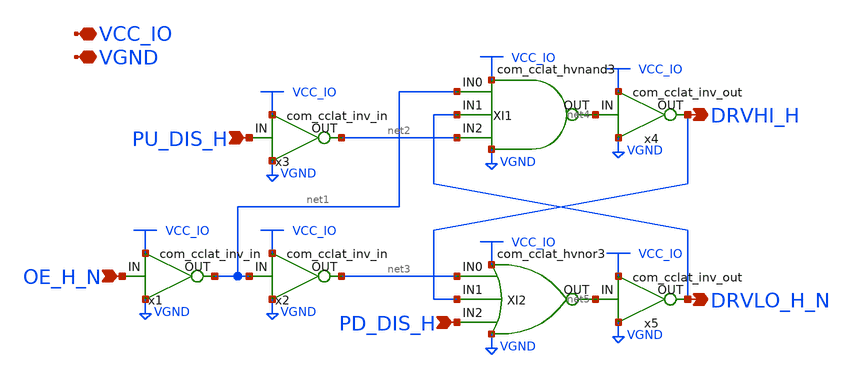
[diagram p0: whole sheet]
** sch_path: com_cclat.sch
* Copyright 2023 David Mitchell Bailey
* Licensed under the Apache License, Version 2.0 (the "License");
* you may not use this file except in compliance with the License.
* You may obtain a copy of the License at
* https://www.apache.org/licenses/LICENSE-2.0
* Unless required by applicable law or agreed to in writing, software
* distributed under the License is distributed on an "AS IS" BASIS,
* WITHOUT WARRANTIES OR CONDITIONS OF ANY KIND, either express or implied.
* See the License for the specific language governing permissions and
* limitations under the License.
**.subckt com_cclat PU_DIS_H VCC_IO DRVHI_H OE_H_N PD_DIS_H DRVLO_H_N VGND
*.ipin PU_DIS_H
*.iopin VCC_IO
*.opin DRVHI_H
*.ipin OE_H_N
*.ipin PD_DIS_H
*.opin DRVLO_H_N
*.iopin VGND
x1 OE_H_N net1 VCC_IO VGND com_cclat_inv_in
x2 net1 net3 VCC_IO VGND com_cclat_inv_in
x3 PU_DIS_H net2 VCC_IO VGND com_cclat_inv_in
XI1 net1 DRVLO_H_N net2 net4 VCC_IO VGND com_cclat_hvnand3
XI2 net3 DRVHI_H PD_DIS_H net5 VCC_IO VGND com_cclat_hvnor3
x4 net4 DRVHI_H VCC_IO VGND com_cclat_inv_out
x5 net5 DRVLO_H_N VCC_IO VGND com_cclat_inv_out
**.ends

* expanding   symbol:  com_cclat_inv_in.sym # of pins=4
** sym_path: com_cclat_inv_in.sym
** sch_path: com_cclat_inv_in.sch
.subckt com_cclat_inv_in IN OUT VCC_IO VGND
*.ipin IN
*.opin OUT
*.iopin VCC_IO
*.iopin VGND
XI1 OUT IN VGND VGND sky130_fd_pr__nfet_g5v0d10v5 L=0.6 W=3 nf=1 ad='int((nf+1)/2) * W/nf * 0.29' as='int((nf+2)/2) * W/nf * 0.29'
+ pd='2*int((nf+1)/2) * (W/nf + 0.29)' ps='2*int((nf+2)/2) * (W/nf + 0.29)' nrd='0.29 / W' nrs='0.29 / W'
+ sa=0 sb=0 sd=0 mult=1 m=1
XI2 OUT IN VCC_IO VCC_IO sky130_fd_pr__pfet_g5v0d10v5 L=0.5 W=5 nf=1 ad='int((nf+1)/2) * W/nf * 0.29'
+ as='int((nf+2)/2) * W/nf * 0.29' pd='2*int((nf+1)/2) * (W/nf + 0.29)' ps='2*int((nf+2)/2) * (W/nf + 0.29)'
+ nrd='0.29 / W' nrs='0.29 / W' sa=0 sb=0 sd=0 mult=1 m=1
.ends


* expanding   symbol:  com_cclat_hvnand3.sym # of pins=6
** sym_path: com_cclat_hvnand3.sym
** sch_path: com_cclat_hvnand3.sch
.subckt com_cclat_hvnand3 IN0 IN1 IN2 OUT VCC_IO VGND
*.ipin IN2
*.opin OUT
*.iopin VCC_IO
*.iopin VGND
*.ipin IN1
*.ipin IN0
XI1 OUT IN2 net1 VGND sky130_fd_pr__nfet_g5v0d10v5 L=0.6 W=3 nf=1 ad='int((nf+1)/2) * W/nf * 0.29' as='int((nf+2)/2) * W/nf * 0.29'
+ pd='2*int((nf+1)/2) * (W/nf + 0.29)' ps='2*int((nf+2)/2) * (W/nf + 0.29)' nrd='0.29 / W' nrs='0.29 / W'
+ sa=0 sb=0 sd=0 mult=2 m=2
XI5 OUT IN2 VCC_IO VCC_IO sky130_fd_pr__pfet_g5v0d10v5 L=0.5 W=5 nf=1 ad='int((nf+1)/2) * W/nf * 0.29'
+ as='int((nf+2)/2) * W/nf * 0.29' pd='2*int((nf+1)/2) * (W/nf + 0.29)' ps='2*int((nf+2)/2) * (W/nf + 0.29)'
+ nrd='0.29 / W' nrs='0.29 / W' sa=0 sb=0 sd=0 mult=1 m=1
XI3 OUT IN1 VCC_IO VCC_IO sky130_fd_pr__pfet_g5v0d10v5 L=0.5 W=5 nf=1 ad='int((nf+1)/2) * W/nf * 0.29'
+ as='int((nf+2)/2) * W/nf * 0.29' pd='2*int((nf+1)/2) * (W/nf + 0.29)' ps='2*int((nf+2)/2) * (W/nf + 0.29)'
+ nrd='0.29 / W' nrs='0.29 / W' sa=0 sb=0 sd=0 mult=1 m=1
XI6 net1 IN1 net2 VGND sky130_fd_pr__nfet_g5v0d10v5 L=0.6 W=3 nf=1 ad='int((nf+1)/2) * W/nf * 0.29' as='int((nf+2)/2) * W/nf * 0.29'
+ pd='2*int((nf+1)/2) * (W/nf + 0.29)' ps='2*int((nf+2)/2) * (W/nf + 0.29)' nrd='0.29 / W' nrs='0.29 / W'
+ sa=0 sb=0 sd=0 mult=2 m=2
XI2 net2 IN0 VGND VGND sky130_fd_pr__nfet_g5v0d10v5 L=0.6 W=3 nf=1 ad='int((nf+1)/2) * W/nf * 0.29' as='int((nf+2)/2) * W/nf * 0.29'
+ pd='2*int((nf+1)/2) * (W/nf + 0.29)' ps='2*int((nf+2)/2) * (W/nf + 0.29)' nrd='0.29 / W' nrs='0.29 / W'
+ sa=0 sb=0 sd=0 mult=4 m=4
XI4 OUT IN0 VCC_IO VCC_IO sky130_fd_pr__pfet_g5v0d10v5 L=0.5 W=5 nf=1 ad='int((nf+1)/2) * W/nf * 0.29'
+ as='int((nf+2)/2) * W/nf * 0.29' pd='2*int((nf+1)/2) * (W/nf + 0.29)' ps='2*int((nf+2)/2) * (W/nf + 0.29)'
+ nrd='0.29 / W' nrs='0.29 / W' sa=0 sb=0 sd=0 mult=1 m=1
.ends


* expanding   symbol:  com_cclat_hvnor3.sym # of pins=6
** sym_path: com_cclat_hvnor3.sym
** sch_path: com_cclat_hvnor3.sch
.subckt com_cclat_hvnor3 IN0 IN1 IN2 OUT VCC_IO VGND
*.ipin IN2
*.opin OUT
*.iopin VCC_IO
*.iopin VGND
*.ipin IN0
*.ipin IN1
XI2 OUT IN2 VGND VGND sky130_fd_pr__nfet_g5v0d10v5 L=0.6 W=3 nf=1 ad='int((nf+1)/2) * W/nf * 0.29' as='int((nf+2)/2) * W/nf * 0.29'
+ pd='2*int((nf+1)/2) * (W/nf + 0.29)' ps='2*int((nf+2)/2) * (W/nf + 0.29)' nrd='0.29 / W' nrs='0.29 / W'
+ sa=0 sb=0 sd=0 mult=2 m=2
XI1 OUT IN2 net1 VCC_IO sky130_fd_pr__pfet_g5v0d10v5 L=0.5 W=5 nf=1 ad='int((nf+1)/2) * W/nf * 0.29'
+ as='int((nf+2)/2) * W/nf * 0.29' pd='2*int((nf+1)/2) * (W/nf + 0.29)' ps='2*int((nf+2)/2) * (W/nf + 0.29)'
+ nrd='0.29 / W' nrs='0.29 / W' sa=0 sb=0 sd=0 mult=4 m=4
XI3 net2 IN0 VCC_IO VCC_IO sky130_fd_pr__pfet_g5v0d10v5 L=0.6 W=5 nf=1 ad='int((nf+1)/2) * W/nf * 0.29'
+ as='int((nf+2)/2) * W/nf * 0.29' pd='2*int((nf+1)/2) * (W/nf + 0.29)' ps='2*int((nf+2)/2) * (W/nf + 0.29)'
+ nrd='0.29 / W' nrs='0.29 / W' sa=0 sb=0 sd=0 mult=8 m=8
XI4 OUT IN0 VGND VGND sky130_fd_pr__nfet_g5v0d10v5 L=0.6 W=3 nf=1 ad='int((nf+1)/2) * W/nf * 0.29' as='int((nf+2)/2) * W/nf * 0.29'
+ pd='2*int((nf+1)/2) * (W/nf + 0.29)' ps='2*int((nf+2)/2) * (W/nf + 0.29)' nrd='0.29 / W' nrs='0.29 / W'
+ sa=0 sb=0 sd=0 mult=2 m=2
XI5 net1 IN1 net2 VCC_IO sky130_fd_pr__pfet_g5v0d10v5 L=0.5 W=5 nf=1 ad='int((nf+1)/2) * W/nf * 0.29'
+ as='int((nf+2)/2) * W/nf * 0.29' pd='2*int((nf+1)/2) * (W/nf + 0.29)' ps='2*int((nf+2)/2) * (W/nf + 0.29)'
+ nrd='0.29 / W' nrs='0.29 / W' sa=0 sb=0 sd=0 mult=4 m=4
XI6 OUT IN1 VGND VGND sky130_fd_pr__nfet_g5v0d10v5 L=0.6 W=3 nf=1 ad='int((nf+1)/2) * W/nf * 0.29' as='int((nf+2)/2) * W/nf * 0.29'
+ pd='2*int((nf+1)/2) * (W/nf + 0.29)' ps='2*int((nf+2)/2) * (W/nf + 0.29)' nrd='0.29 / W' nrs='0.29 / W'
+ sa=0 sb=0 sd=0 mult=2 m=2
.ends


* expanding   symbol:  com_cclat_inv_out.sym # of pins=4
** sym_path: com_cclat_inv_out.sym
** sch_path: com_cclat_inv_out.sch
.subckt com_cclat_inv_out IN OUT VCC_IO VGND
*.ipin IN
*.opin OUT
*.iopin VCC_IO
*.iopin VGND
XI1 OUT IN VGND VGND sky130_fd_pr__nfet_g5v0d10v5 L=0.6 W=3 nf=1 ad='int((nf+1)/2) * W/nf * 0.29' as='int((nf+2)/2) * W/nf * 0.29'
+ pd='2*int((nf+1)/2) * (W/nf + 0.29)' ps='2*int((nf+2)/2) * (W/nf + 0.29)' nrd='0.29 / W' nrs='0.29 / W'
+ sa=0 sb=0 sd=0 mult=6 m=6
XI2 OUT IN VCC_IO VCC_IO sky130_fd_pr__pfet_g5v0d10v5 L=0.5 W=5 nf=1 ad='int((nf+1)/2) * W/nf * 0.29'
+ as='int((nf+2)/2) * W/nf * 0.29' pd='2*int((nf+1)/2) * (W/nf + 0.29)' ps='2*int((nf+2)/2) * (W/nf + 0.29)'
+ nrd='0.29 / W' nrs='0.29 / W' sa=0 sb=0 sd=0 mult=6 m=6
.ends

.end
